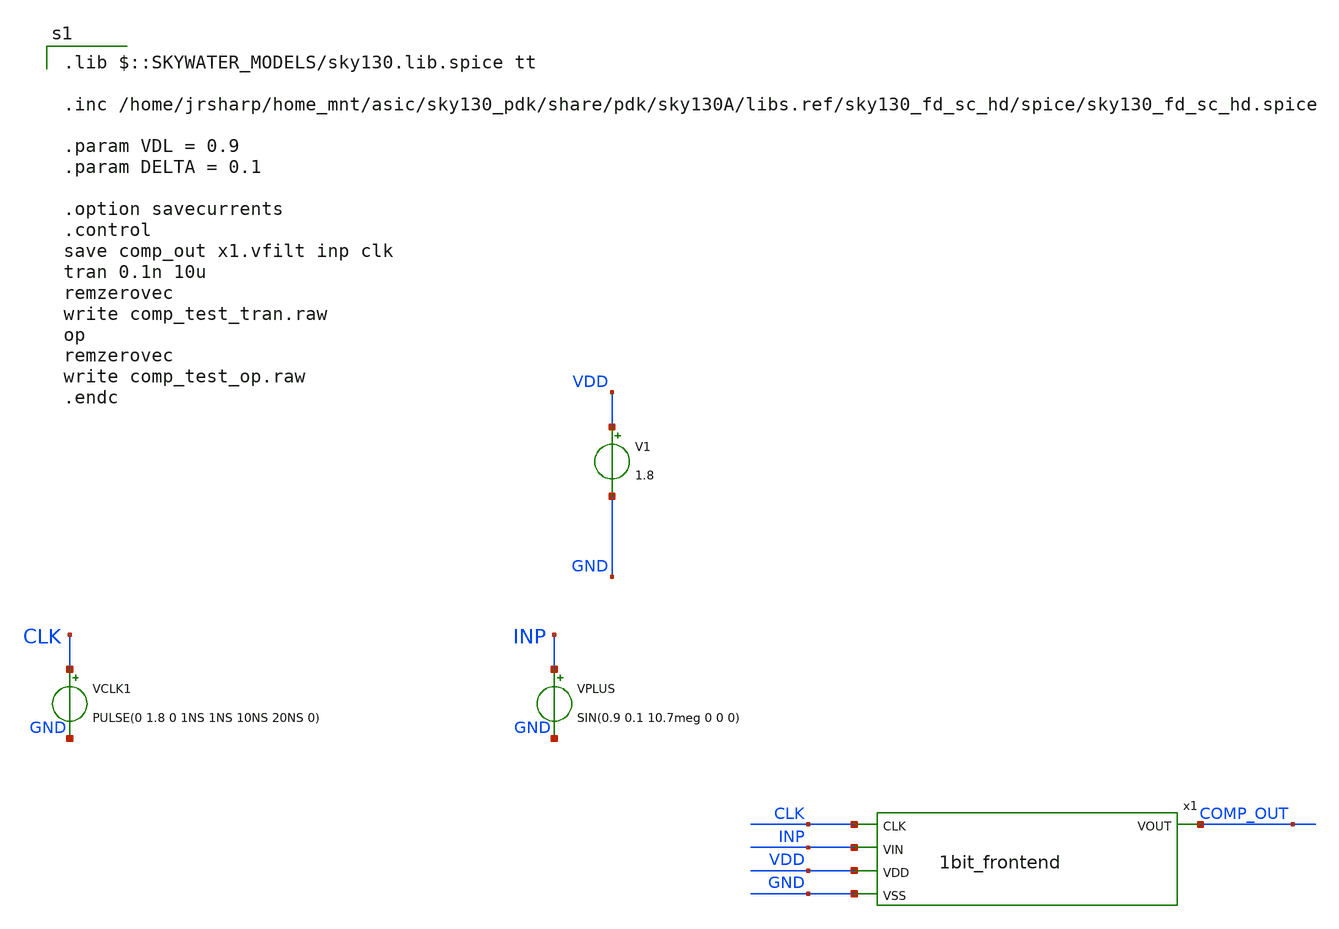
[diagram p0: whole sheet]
** sch_path: xschem/1bit_frontent_test.sch
**.subckt 1bit_frontent_test
V1 VDD GND 1.8
VPLUS INP GND SIN(0.9 0.1 10.7meg 0 0 0)
VCLK1 CLK GND PULSE(0 1.8 0 1NS 1NS 10NS 20NS 0)
x1 COMP_OUT CLK INP VDD GND 1bit_frontend
**** begin user architecture code
 .lib $::SKYWATER_MODELS/sky130.lib.spice tt

.inc /home/jrsharp/home_mnt/asic/sky130_pdk/share/pdk/sky130A/libs.ref/sky130_fd_sc_hd/spice/sky130_fd_sc_hd.spice

.param VDL = 0.9
.param DELTA = 0.1

.option savecurrents
.control
save comp_out x1.vfilt inp clk
tran 0.1n 10u
remzerovec
write comp_test_tran.raw
op
remzerovec
write comp_test_op.raw
.endc



**** end user architecture code
**.ends
.end
